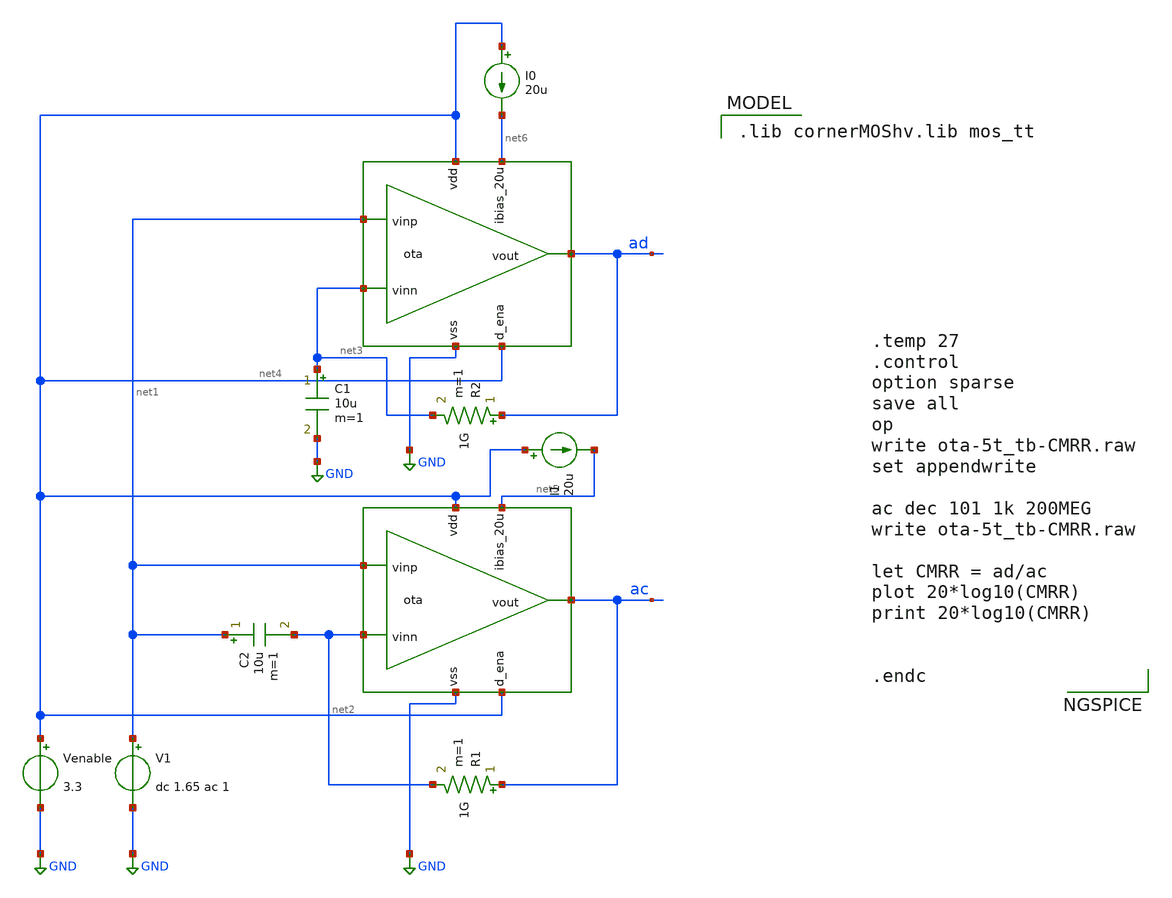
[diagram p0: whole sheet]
** sch_path: Differntial_Amp/design_data/xschem/ota-5t_tb-cmrr.sch
**.subckt ota-5t_tb-cmrr
x1 net4 ac net1 net2 net5 GND net4 ota
V1 net1 GND dc 1.65 ac 1
x2 net4 ad net1 net3 net6 GND net4 ota
R1 ac net2 1G m=1
R2 ad net3 1G m=1
C1 net3 GND 10u m=1
C2 net1 net2 10u m=1
Venable net4 GND 3.3
I0 net4 net6 20u
I1 net4 net5 20u
**** begin user architecture code
 .lib cornerMOShv.lib mos_tt



.temp 27
.control
option sparse
save all
op
write ota-5t_tb-CMRR.raw
set appendwrite

ac dec 101 1k 200MEG
write ota-5t_tb-CMRR.raw

let CMRR = ad/ac
plot 20*log10(CMRR)
print 20*log10(CMRR)


.endc


**** end user architecture code
**.ends

* expanding   symbol:
*+  /home/aidas93/Downloads/TO_Nov2024-main/Differntial_Amp/design_data/xschem/ota.sym # of pins=7
** sym_path: Differntial_Amp/design_data/xschem/ota.sym
** sch_path: Differntial_Amp/design_data/xschem/ota.sch
.subckt ota vdd vout vinp vinn ibias_20u vss d_ena
*.opin vout
*.iopin vdd
*.iopin vss
*.ipin ibias_20u
*.ipin vinn
*.ipin vinp
*.ipin d_ena
XM1 vout vinn net2 vss sg13_hv_nmos w=0.53u l=1u ng=1 m=4 mm_ok=1
XM2 net1 vinp net2 vss sg13_hv_nmos w=0.53u l=1u ng=1 m=4 mm_ok=1
XM5 net2 net3 vss vss sg13_hv_nmos w=0.76u l=1u ng=1 m=1 mm_ok=1
XM3 net1 net1 vdd vdd sg13_hv_pmos w=1.45u l=1u ng=1 m=1 mm_ok=1
XM4 vout net1 vdd vdd sg13_hv_pmos w=1.45u l=1u ng=1 m=1 mm_ok=1
XM6 ibias_20u net3 vss vss sg13_hv_nmos w=3.075u l=1u ng=5 m=1 mm_ok=1
XM7 net1 d_ena vdd vdd sg13_hv_pmos w=1.5u l=1u ng=1 m=1 mm_ok=1
XM8 net4 d_ena vdd vdd sg13_hv_pmos w=1.5u l=1u ng=1 m=1 mm_ok=1
XM9 ibias_20u net4 net3 vss sg13_hv_nmos w=0.5u l=1u ng=1 m=1 mm_ok=1
XM10 net3 net4 vss vss sg13_hv_nmos w=0.5u l=1u ng=1 m=1 mm_ok=1
XM11 net4 d_ena vss vss sg13_hv_nmos w=0.5u l=1u ng=1 m=1 mm_ok=1
XM12 vss vss vss vss sg13_hv_nmos w=0.5u l=0.5u ng=1 m=1 mm_ok=1
XM13 vss vss vss vss sg13_hv_nmos w=0.5u l=0.5u ng=1 m=1 mm_ok=1
XM14 vss vss vss vss sg13_hv_nmos w=0.76u l=0.5u ng=1 m=1 mm_ok=1
XM15 vss vss vss vss sg13_hv_nmos w=0.615u l=0.5u ng=1 m=1 mm_ok=1
XM16 vss vss vss vss sg13_hv_nmos w=0.615u l=0.5u ng=1 m=1 mm_ok=1
XM17 vss vss vss vss sg13_hv_nmos w=0.76u l=0.5u ng=1 m=1 mm_ok=1
XM18 vss vss vss vss sg13_hv_nmos w=0.5u l=0.5u ng=1 m=1 mm_ok=1
XM19 vss vss vss vss sg13_hv_nmos w=0.5u l=0.5u ng=1 m=1 mm_ok=1
XM20 vss vss vss vss sg13_hv_nmos w=0.53u l=0.5u ng=1 m=1 mm_ok=1
XM21 vss vss vss vss sg13_hv_nmos w=0.53u l=0.5u ng=1 m=1 mm_ok=1
XM22 vss vss vss vss sg13_hv_nmos w=0.53u l=0.5u ng=1 m=1 mm_ok=1
XM23 vss vss vss vss sg13_hv_nmos w=0.53u l=0.5u ng=1 m=1 mm_ok=1
XM24 vss vss vss vss sg13_hv_nmos w=0.5u l=1u ng=1 m=1 mm_ok=1
XM25 vss vss vss vss sg13_hv_nmos w=0.5u l=1u ng=1 m=1 mm_ok=1
XM26 vss vss vss vss sg13_hv_nmos w=0.5u l=0.5u ng=1 m=1 mm_ok=1
XM27 vss vss vss vss sg13_hv_nmos w=0.5u l=0.5u ng=1 m=1 mm_ok=1
XM28 vss vss vss vss sg13_hv_nmos w=0.53u l=0.5u ng=1 m=1 mm_ok=1
XM29 vss vss vss vss sg13_hv_nmos w=0.53u l=0.5u ng=1 m=1 mm_ok=1
XM30 vss vss vss vss sg13_hv_nmos w=0.53u l=0.5u ng=1 m=1 mm_ok=1
XM31 vss vss vss vss sg13_hv_nmos w=0.53u l=0.5u ng=1 m=1 mm_ok=1
XM32 vss vss vss vss sg13_hv_nmos w=0.5u l=1u ng=1 m=1 mm_ok=1
XM33 vss vss vss vss sg13_hv_nmos w=0.5u l=1u ng=1 m=1 mm_ok=1
XM34 vdd vdd vdd vdd sg13_hv_pmos w=1.45u l=0.5u ng=1 m=1 mm_ok=1
XM35 vdd vdd vdd vdd sg13_hv_pmos w=1.45u l=0.5u ng=1 m=1 mm_ok=1
XM36 vdd vdd vdd vdd sg13_hv_pmos w=1.45u l=0.5u ng=1 m=1 mm_ok=1
XM37 vdd vdd vdd vdd sg13_hv_pmos w=1.45u l=0.5u ng=1 m=1 mm_ok=1
.ends

.GLOBAL GND
.end
